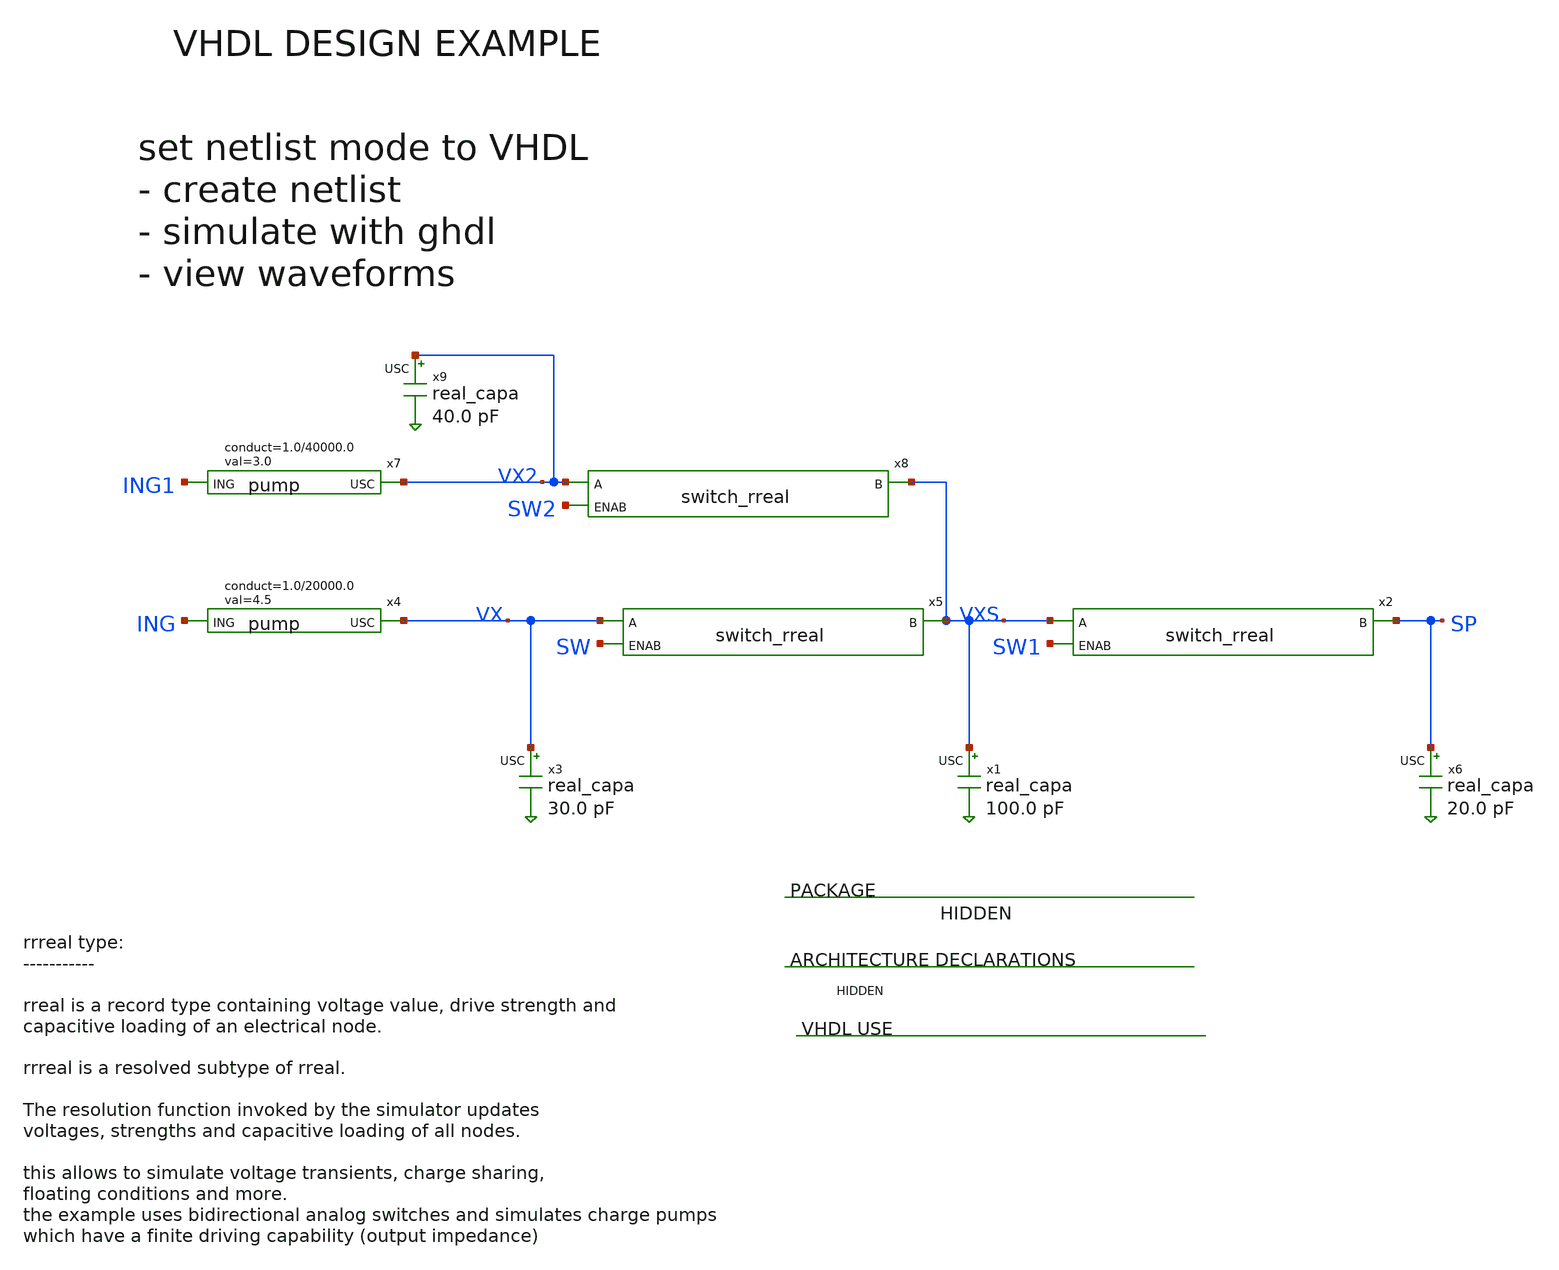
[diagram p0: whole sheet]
** sch_path: library/examples/loading.sch
**.subckt loading
x4 VX ING pump
x5 SW VXS VX switch_rreal
x3 VX real_capa
x1 VXS real_capa
x2 SW1 SP VXS switch_rreal
x6 SP real_capa
x7 VX2 ING1 pump
x8 SW2 VXS VX2 switch_rreal
x9 VX2 real_capa
**** begin user architecture code
* test
**** end user architecture code
**.ends
.end
